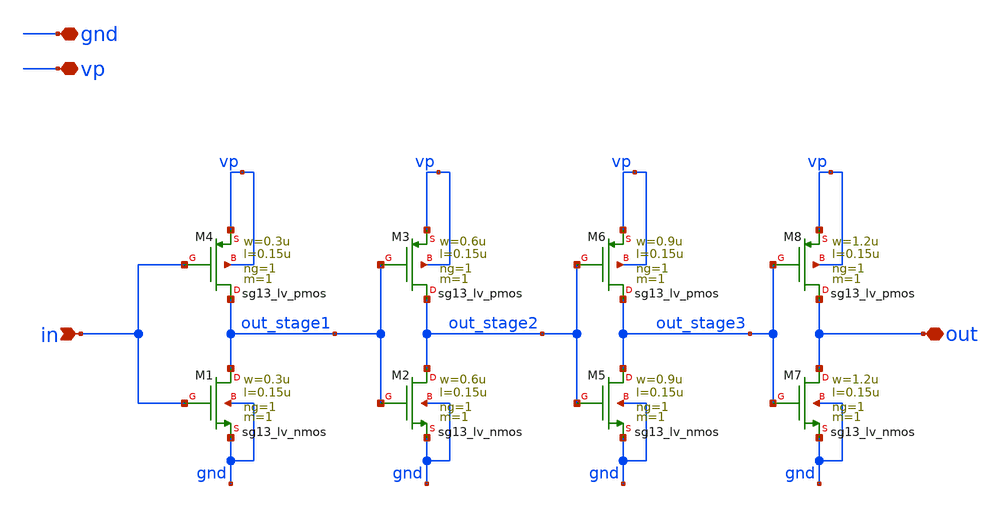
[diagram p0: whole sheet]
** sch_path: PFD/PFD_buffor.sch
**.subckt PFD_buffor gnd vp in out
*.iopin gnd
*.iopin vp
*.ipin in
*.iopin out
XM1 out_stage1 in gnd gnd sg13_lv_nmos w=0.3u l=0.15u ng=1 m=1 mm_ok=1
XM4 out_stage1 in vp vp sg13_lv_pmos w=0.3u l=0.15u ng=1 m=1 mm_ok=1
XM2 out_stage2 out_stage1 gnd gnd sg13_lv_nmos w=0.6u l=0.15u ng=1 m=1 mm_ok=1
XM3 out_stage2 out_stage1 vp vp sg13_lv_pmos w=0.6u l=0.15u ng=1 m=1 mm_ok=1
XM5 out_stage3 out_stage2 gnd gnd sg13_lv_nmos w=0.9u l=0.15u ng=1 m=1 mm_ok=1
XM6 out_stage3 out_stage2 vp vp sg13_lv_pmos w=0.9u l=0.15u ng=1 m=1 mm_ok=1
XM7 out out_stage3 gnd gnd sg13_lv_nmos w=1.2u l=0.15u ng=1 m=1 mm_ok=1
XM8 out out_stage3 vp vp sg13_lv_pmos w=1.2u l=0.15u ng=1 m=1 mm_ok=1
**.ends
.end
